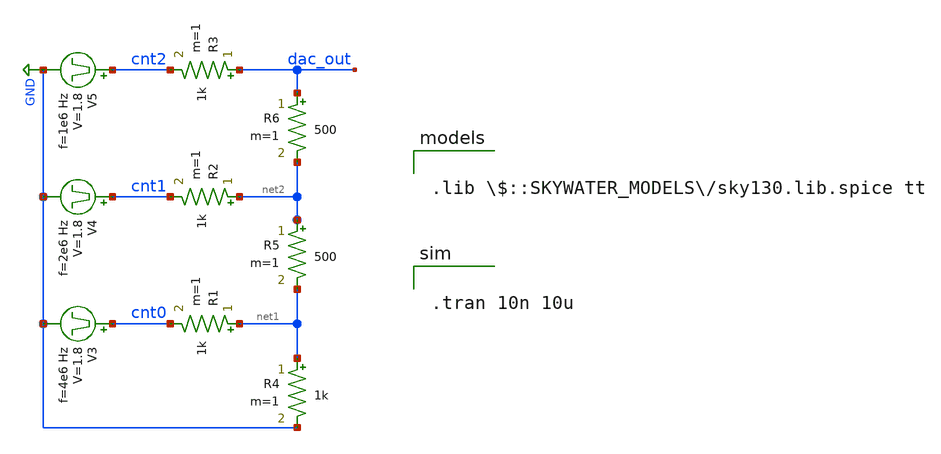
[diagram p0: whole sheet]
** sch_path: design/playground/r-2r_1v8_tb.sch
**.subckt r-2r_1v8_tb
V3 cnt0 GND pulse 0 1.8 '0.495/ 4e6 ' '0.01/4e6 ' '0.01/4e6 ' '0.49/4e6 ' '1/4e6 '
V4 cnt1 GND pulse 0 1.8 '0.495/ 2e6 ' '0.01/2e6 ' '0.01/2e6 ' '0.49/2e6 ' '1/2e6 '
V5 cnt2 GND pulse 0 1.8 '0.495/ 1e6 ' '0.01/1e6 ' '0.01/1e6 ' '0.49/1e6 ' '1/1e6 '
R1 net1 cnt0 1k m=1
R2 net2 cnt1 1k m=1
R3 dac_out cnt2 1k m=1
R4 net1 GND 1k m=1
R5 net2 net1 500 m=1
R6 dac_out net2 500 m=1
**** begin user architecture code


.tran 10n 10u



.lib $::SKYWATER_MODELS/sky130.lib.spice tt

**** end user architecture code
**.ends
.GLOBAL GND
.end
